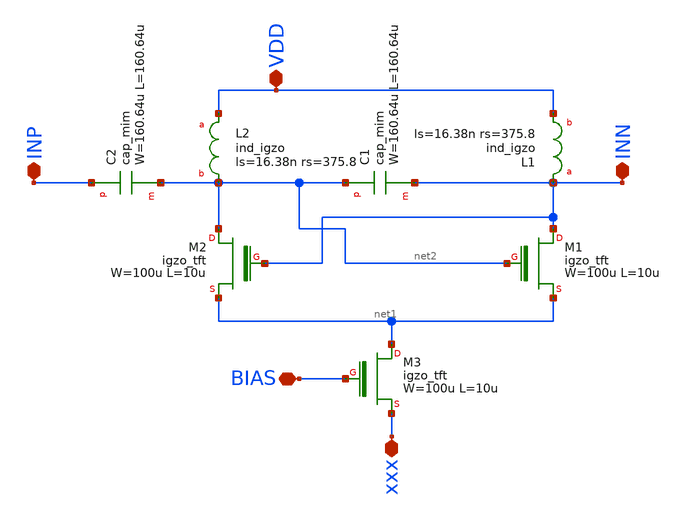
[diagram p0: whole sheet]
** sch_path: 100X/XSCHEM/BASIC_CELL.sch
**.subckt BASIC_CELL VDD xxx INP INN BIAS
*.iopin VDD
*.iopin xxx
*.iopin INP
*.iopin INN
*.iopin BIAS
XC1 net2 INN cap_mim W=160.64u L=160.64u
XL1 INN VDD ind_igzo ls=16.38n rs=375.8
XM1 INN net2 net1 igzo_tft W=100u L=10u ov=5u nf=1 m=1
XM2 net2 INN net1 igzo_tft W=100u L=10u ov=5u nf=1 m=1
XL2 VDD net2 ind_igzo ls=16.38n rs=375.8
XC2 INP net2 cap_mim W=160.64u L=160.64u
XM3 net1 BIAS xxx igzo_tft W=100u L=10u ov=5u nf=1 m=1
**.ends
.end
